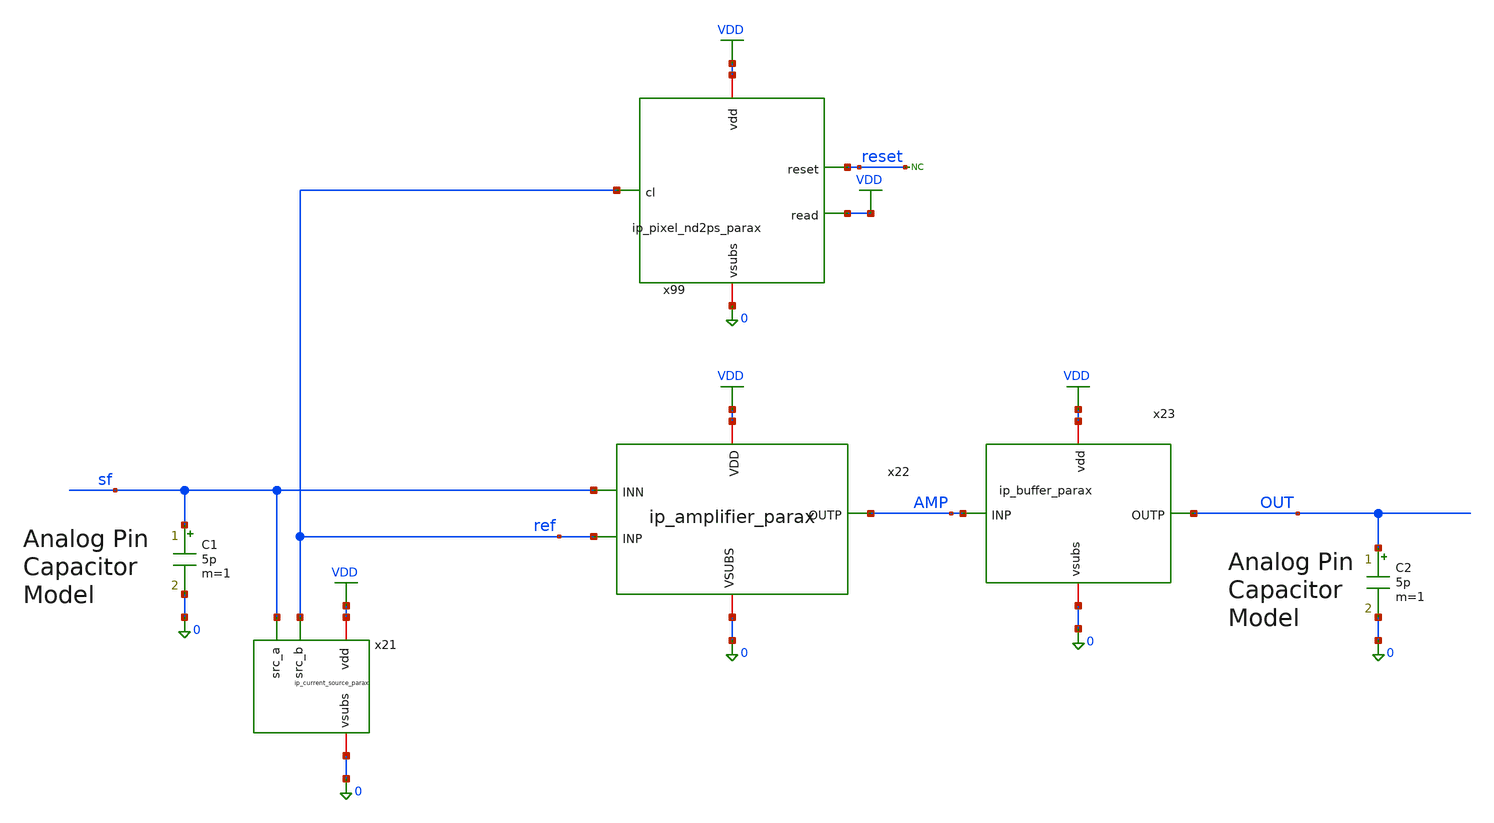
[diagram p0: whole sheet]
** sch_path: xschem/tb_total_tran.sch
**.subckt tb_total_tran
x21 VDD sf 0 ref ip_current_source_parax
x22 VDD AMP ref sf 0 ip_amplifier_parax
x99 VDD reset VDD 0 ref ip_pixel_nd2ps_parax
C1 sf 0 5p m=1
x23 VDD OUT AMP 0 ip_buffer_parax
C2 OUT 0 5p m=1
* noconn reset
**** begin user architecture code

.include $::180MCU_MODELS/design.ngspice
.lib $::180MCU_MODELS/sm141064.ngspice typical
.lib $::180MCU_MODELS/sm141064.ngspice res_typical
.lib $::180MCU_MODELS/sm141064.ngspice moscap_typical
.lib $::180MCU_MODELS/sm141064.ngspice diode_typical




.options reltol=0.005 vntol=10u abstol=10n
.control
	reset
	tran 1u 1.8m
	write tb_total_tran.raw
	quit
.endc






VVDD VDD 0 3.3
VCLK CLK 0 PULSE (0 3.3 5u 1n 1n 5u 10u)

astim [RESETA        dRA4 dRA3 dRA2 dRA1 dRA0        dCA4 dCA3 dCA2 dCA1 dCA0] stim
.model stim d_source input_file="../st_total.txt"

acosim[CLK        dCA4 dCA3 dCA2 dCA1 dCA0        dRA4 dRA3 dRA2 dRA1 dRA0        RESETA]
+        [dreset        dCY20 dCY19 dCY18 dCY17 dCY16 dCY15        dCY14 dCY13 dCY12 dCY11 dCY10 dCY9         dCY8
+  dCY7  dCY6  dCY5  dCY4  dCY3         dCY2  dCY1  dCY0         dRY16 dRY15 dRY14 dRY13 dRY12 dRY11
+         dRY10 dRY9  dRY8  dRY7  dRY6  dRY5        dRY4  dRY3  dRY2  dRY1  dRY0        ] null dut
.model dut d_cosim simulation="../../verilog/rtl/aux_total_digital/aux_total_digital.so"

.include pixels.spice


**** end user architecture code
**.ends

* expanding   symbol:  ip_current_source_parax.sym # of pins=4
** sym_path: xschem/ip_current_source.sym
.include [file normalize ./parax/ip_current_source.sim.spice]

* expanding   symbol:  ip_amplifier_parax.sym # of pins=5
** sym_path: xschem/ip_amplifier.sym
.include [file normalize ./parax/ip_amplifier.sim.spice]

* expanding   symbol:  ip_pixel_nd2ps_parax.sym # of pins=5
** sym_path: xschem/ip_pixel_nd2ps.sym
.include [file normalize ./parax/ip_pixel_nd2ps.sim.spice]

* expanding   symbol:  ip_buffer_parax.sym # of pins=4
** sym_path: xschem/ip_buffer.sym
.include [file normalize ./parax/ip_buffer.sim.spice]
.GLOBAL VDD
.end
